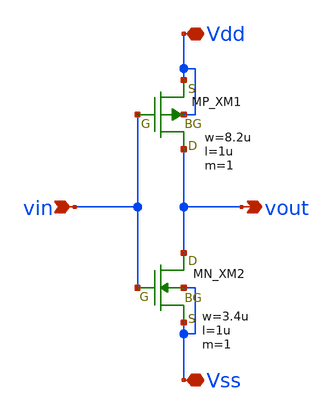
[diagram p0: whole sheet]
** sch_path: member_project/inverter/OpenSUSI/makoto56/inverter_makoto56.sch
**.subckt inverter_makoto56 vin Vdd vout Vss
*.ipin vin
*.iopin Vdd
*.opin vout
*.iopin Vss
XXM1 vout vin Vdd Vdd PMOS w=8.2u l=1u nrd=0 nrs=0 m=1
XXM2 vout vin Vss Vss NMOS w=3.4u l=1u nrd=0 nrs=0 m=1
**.ends
.end
